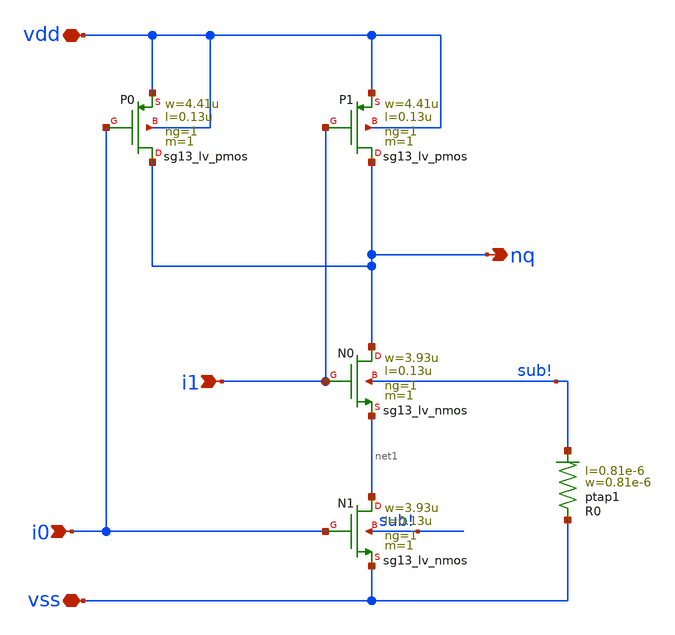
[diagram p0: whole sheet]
** sch_path: ihp-sg13g2/libs.ref/sg13g2_io/sch/xschem/sg13g2_io_nand2_x1.sch
**.subckt sg13g2_io_nand2_x1 i0 i1 vdd vss nq
*.ipin i0
*.ipin i1
*.iopin vdd
*.iopin vss
*.opin nq
XN0 nq i1 net1 sub! sg13_lv_nmos w=3.93u l=0.13u ng=1 m=1 mm_ok=1
XN1 net1 i0 vss sub! sg13_lv_nmos w=3.93u l=0.13u ng=1 m=1 mm_ok=1
XP0 nq i0 vdd vdd sg13_lv_pmos w=4.41u l=0.13u ng=1 m=1 mm_ok=1
XP1 nq i1 vdd vdd sg13_lv_pmos w=4.41u l=0.13u ng=1 m=1 mm_ok=1
XR0 vss sub! ptap1 R=251.5 w=0.81e-6 l=0.81e-6
**.ends
.end
